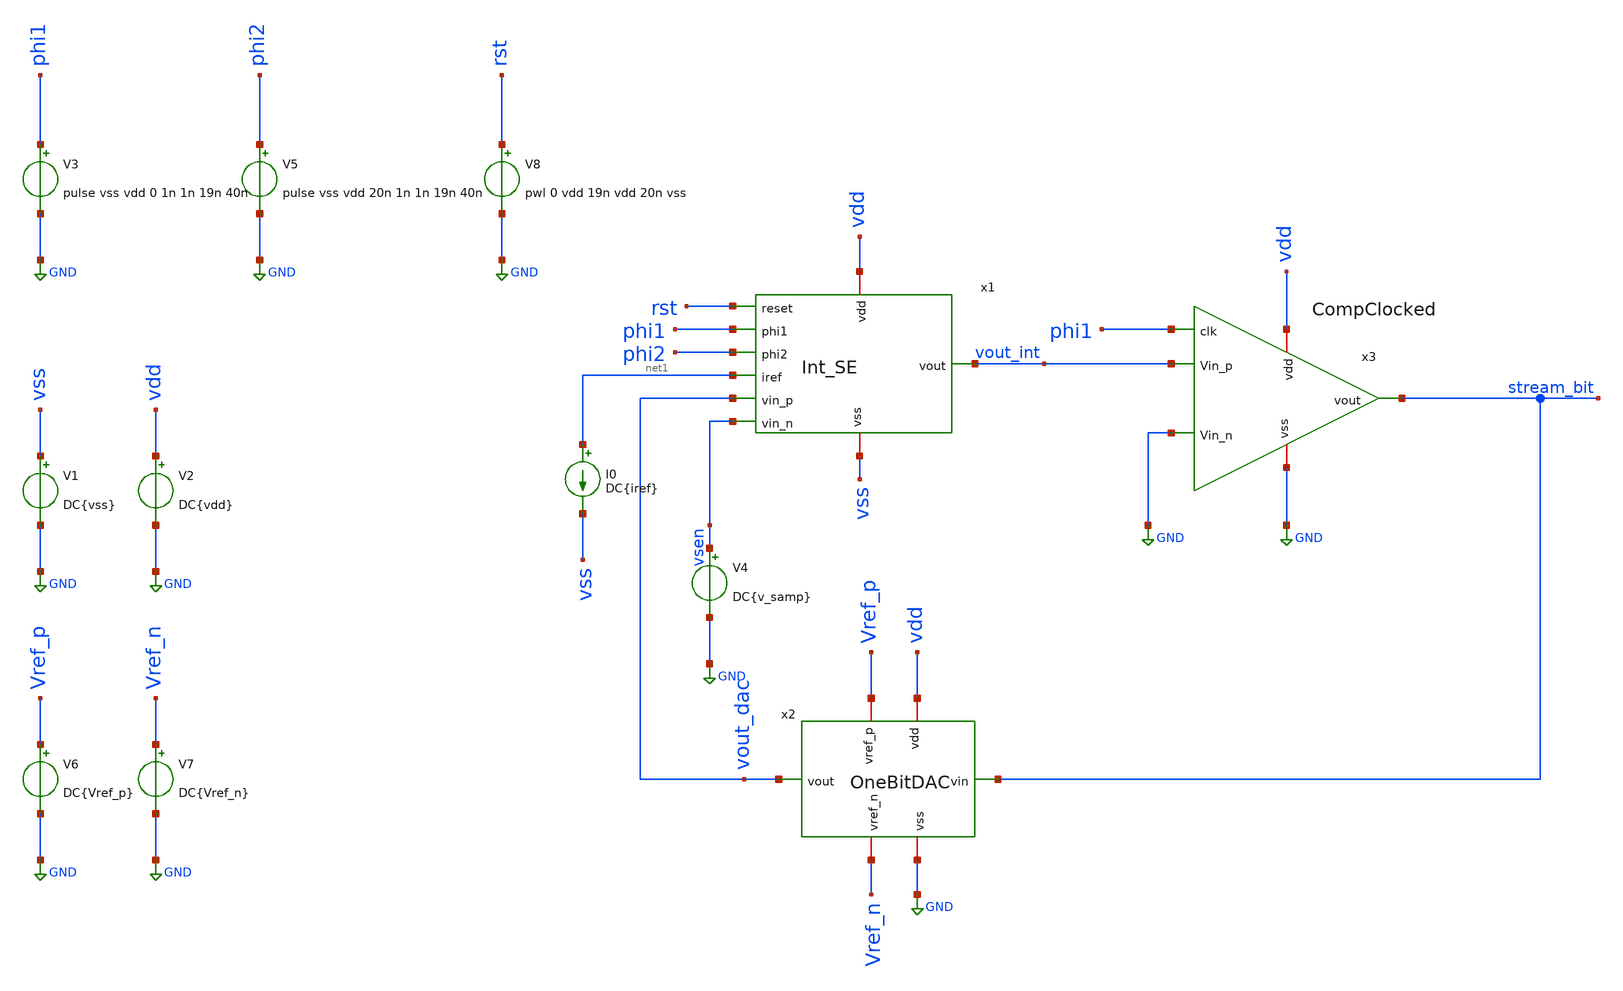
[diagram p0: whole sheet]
** sch_path: xschem/SigmaDelta_tb.sch

.lib $::SKYWATER_MODELS/sky130.lib.spice tt
.include $::SKYWATER_STDCELLS/sky130_fd_sc_hd.spice

**.subckt SigmaDelta_tb
V1 vss GND DC{vss}
V2 vdd GND DC{vdd}
I0 net1 vss DC{iref}
V3 phi1 GND pulse vss vdd 0 1n 1n 19n 40n
V5 phi2 GND pulse vss vdd 20n 1n 1n 19n 40n
x2 Vref_p vdd stream_bit vout_dac Vref_n GND OneBitDAC
V6 Vref_p GND DC{Vref_p}
V7 Vref_n GND DC{Vref_n}
x1 rst phi1 vdd vsen vout_int net1 phi2 vss vout_dac Int_SE
x3 vdd phi1 stream_bit GND vout_int GND CompClocked
V8 rst GND pwl 0 vdd 19n vdd 20n vss
V4 vsen GND DC{v_samp}
**** begin user architecture code

* this option enables mos model bin
* selection based on W/NF instead of W
.option wnflag=1
.option savecurrents

* Circuit Parameters
.param iref = 100u
.param vdd  = 1.8
.param vss  = -1.8
.param Vref_p = 1.5
.param Vref_n = 0
.param v_samp = 0.25
.options TEMP = 65.0

* OP Parameters & Singals to save
.save all

*Simulations
.control
  save v(x2.VINV)
  tran 0.1n 500n
  setplot tran1
  plot v(vsen) v(vout_Int) v(phi1) v(phi2) v(vout_dac)
  write /foss/designs/SigmaDelta_ADC/xschem/sim_results/SigmaDelta.raw
.endc

.end


**** end user architecture code
**.ends
.GLOBAL GND
.end
